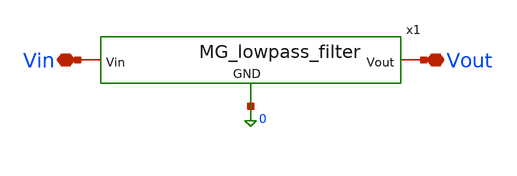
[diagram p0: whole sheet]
** sch_path: MG_filter/MG_lowpass_filter_testbench.sch
**.subckt MG_lowpass_filter_testbench Vout Vin
*.iopin Vout
*.iopin Vin
x1 Vin Vout 0 MG_lowpass_filter
**** begin user architecture code


.include /foss/pdks/gf180mcuD/libs.tech/ngspice/design.ngspice
.lib /foss/pdks/gf180mcuD/libs.tech/ngspice/sm141064.ngspice typical
.lib /foss/pdks/gf180mcuD/libs.tech/ngspice/sm141064.ngspice res_typical
.lib /foss/pdks/gf180mcuD/libs.tech/ngspice/sm141064.ngspice mimcap_typical
.lib /foss/pdks/gf180mcuD/libs.tech/ngspice/sm141064.ngspice cap_mim

Vin Vin 0 DC 0 AC 1 PULSE(0 1 10p 10p 10p 50n 100n)

.control
  save v(Vin) v(Vout)

  * --- AC Analysis ---
  ac dec 50 1Hz 1GHz
  let vout = v(Vout)
  let vout_db = db(v(Vout))
  let vout_phase = ph(v(Vout)) * 180 / PI
  meas ac f_3db WHEN vout_db = -3 FALL=1
  plot vout vs frequency xlabel 'Frequency [Hz]' ylabel 'Gain' title 'GF180MCU Gain Response'
  plot vout_db vs frequency xlabel 'Frequency [Hz]' ylabel 'Gain [dB]' title 'GF180MCU Gain Response in dB'
  plot vout_phase vs frequency xlabel 'Frequency [Hz]' ylabel 'Phase [deg]' title 'GF180MCU Phase Response'

  * --- Transient Analysis ---
  tran 10n 1000n
  plot v(Vin) v(Vout) xlabel 'Time [s]' ylabel 'Voltage [V]' title 'GF180MCU Step Response'
.endc


**** end user architecture code
**.ends
.end
